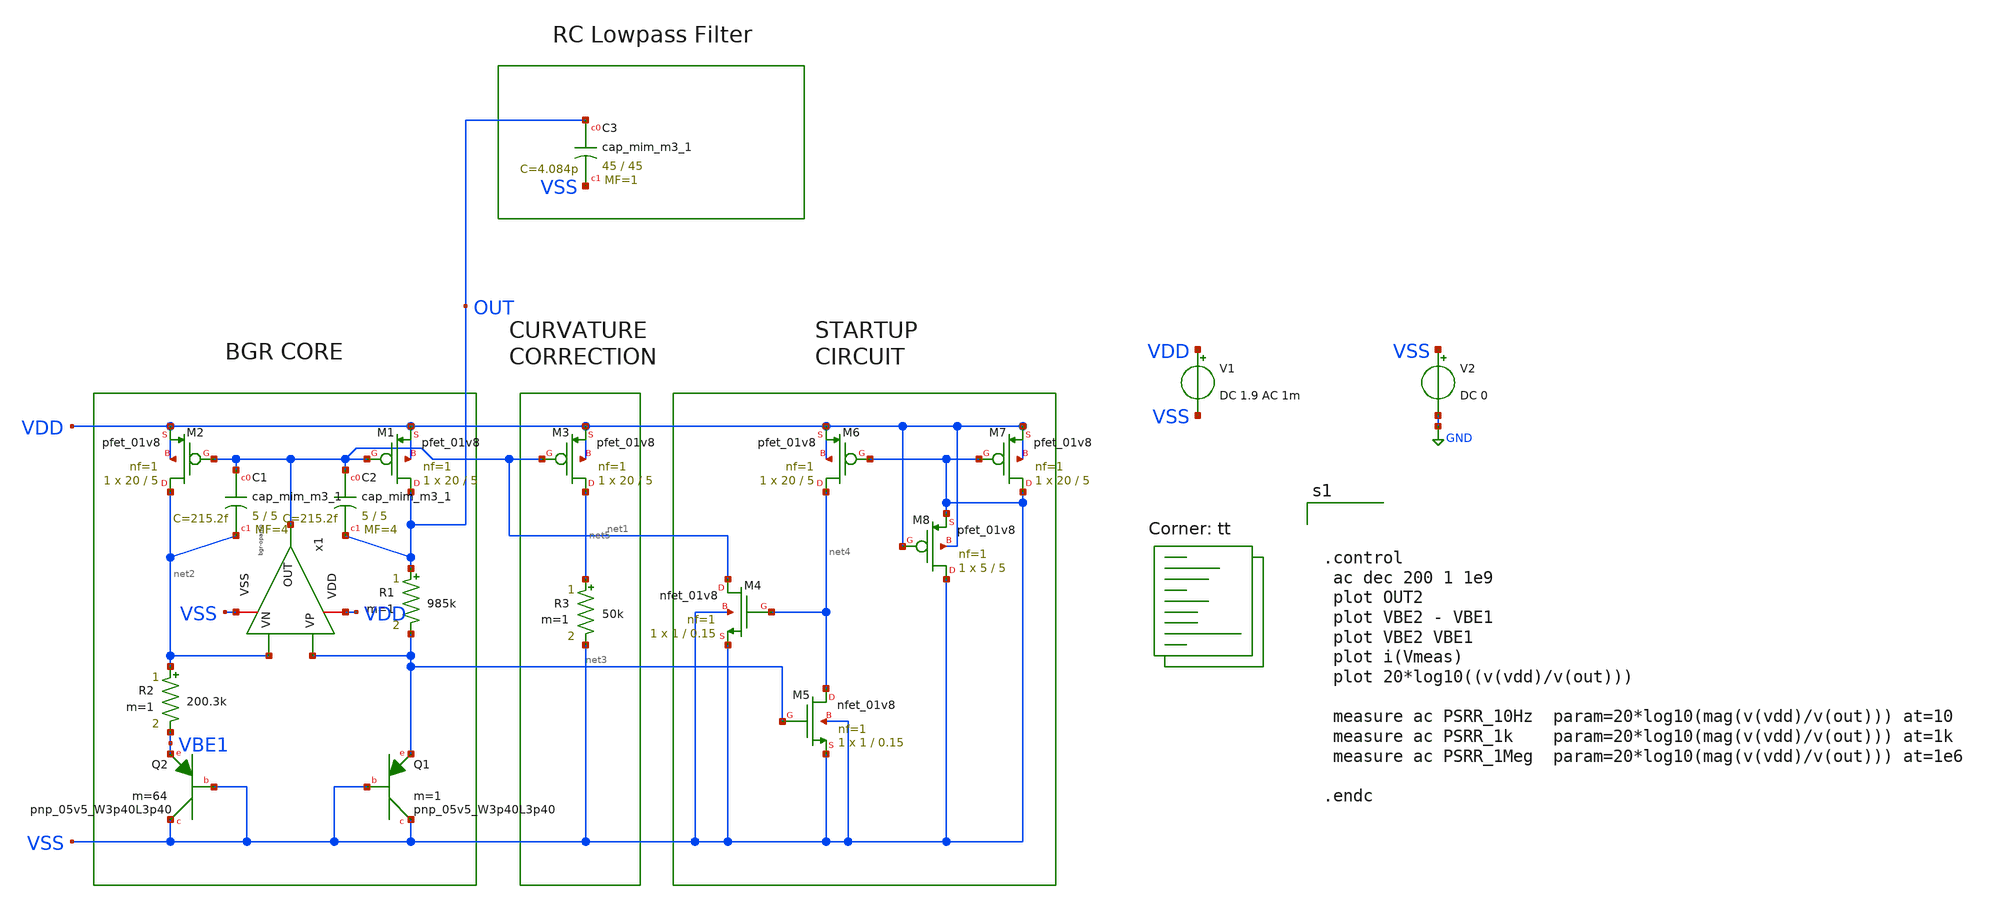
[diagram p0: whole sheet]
** sch_path: bandgap/bgr2-ac.sch
**.subckt bgr2-ac
XM1 OUT net1 VDD VDD sky130_fd_pr__pfet_01v8 L=5 W=20 nf=1 ad='int((nf+1)/2) * W/nf * 0.29' as='int((nf+2)/2) * W/nf * 0.29'
+ pd='2*int((nf+1)/2) * (W/nf + 0.29)' ps='2*int((nf+2)/2) * (W/nf + 0.29)' nrd='0.29 / W' nrs='0.29 / W'
+ sa=0 sb=0 sd=0 mult=1 m=1
XM2 net2 net1 VDD VDD sky130_fd_pr__pfet_01v8 L=5 W=20 nf=1 ad='int((nf+1)/2) * W/nf * 0.29' as='int((nf+2)/2) * W/nf * 0.29'
+ pd='2*int((nf+1)/2) * (W/nf + 0.29)' ps='2*int((nf+2)/2) * (W/nf + 0.29)' nrd='0.29 / W' nrs='0.29 / W'
+ sa=0 sb=0 sd=0 mult=1 m=1
R1 OUT net3 985k m=1
R2 net2 VBE1 200.3k m=1
XQ1 VSS VSS net3 sky130_fd_pr__pnp_05v5_W3p40L3p40 m=1
XQ2 VSS VSS VBE1 sky130_fd_pr__pnp_05v5_W3p40L3p40 m=64
V1 VDD VSS DC 1.9 AC 1m
V2 VSS GND DC 0
XM3 net5 net1 VDD VDD sky130_fd_pr__pfet_01v8 L=5 W=20 nf=1 ad='int((nf+1)/2) * W/nf * 0.29' as='int((nf+2)/2) * W/nf * 0.29'
+ pd='2*int((nf+1)/2) * (W/nf + 0.29)' ps='2*int((nf+2)/2) * (W/nf + 0.29)' nrd='0.29 / W' nrs='0.29 / W'
+ sa=0 sb=0 sd=0 mult=1 m=1
R3 net5 VSS 50k m=1
XM4 net1 net4 VSS VSS sky130_fd_pr__nfet_01v8 L=0.15 W=1 nf=1 ad='int((nf+1)/2) * W/nf * 0.29' as='int((nf+2)/2) * W/nf * 0.29'
+ pd='2*int((nf+1)/2) * (W/nf + 0.29)' ps='2*int((nf+2)/2) * (W/nf + 0.29)' nrd='0.29 / W' nrs='0.29 / W'
+ sa=0 sb=0 sd=0 mult=1 m=1
XM5 net4 net3 VSS VSS sky130_fd_pr__nfet_01v8 L=0.15 W=1 nf=1 ad='int((nf+1)/2) * W/nf * 0.29' as='int((nf+2)/2) * W/nf * 0.29'
+ pd='2*int((nf+1)/2) * (W/nf + 0.29)' ps='2*int((nf+2)/2) * (W/nf + 0.29)' nrd='0.29 / W' nrs='0.29 / W'
+ sa=0 sb=0 sd=0 mult=1 m=1
XM6 net4 VSS VDD VDD sky130_fd_pr__pfet_01v8 L=5 W=20 nf=1 ad='int((nf+1)/2) * W/nf * 0.29' as='int((nf+2)/2) * W/nf * 0.29'
+ pd='2*int((nf+1)/2) * (W/nf + 0.29)' ps='2*int((nf+2)/2) * (W/nf + 0.29)' nrd='0.29 / W' nrs='0.29 / W'
+ sa=0 sb=0 sd=0 mult=1 m=1
XM7 VSS VSS VDD VDD sky130_fd_pr__pfet_01v8 L=5 W=20 nf=1 ad='int((nf+1)/2) * W/nf * 0.29' as='int((nf+2)/2) * W/nf * 0.29'
+ pd='2*int((nf+1)/2) * (W/nf + 0.29)' ps='2*int((nf+2)/2) * (W/nf + 0.29)' nrd='0.29 / W' nrs='0.29 / W'
+ sa=0 sb=0 sd=0 mult=1 m=1
XM8 VSS VDD VSS VDD sky130_fd_pr__pfet_01v8 L=5 W=5 nf=1 ad='int((nf+1)/2) * W/nf * 0.29' as='int((nf+2)/2) * W/nf * 0.29'
+ pd='2*int((nf+1)/2) * (W/nf + 0.29)' ps='2*int((nf+2)/2) * (W/nf + 0.29)' nrd='0.29 / W' nrs='0.29 / W'
+ sa=0 sb=0 sd=0 mult=1 m=1
x1 VDD net1 net3 net2 VSS bgr-opamp
XC1 net1 net2 sky130_fd_pr__cap_mim_m3_1 W=5 L=5 MF=4 m=4
XC2 net1 OUT sky130_fd_pr__cap_mim_m3_1 W=5 L=5 MF=4 m=4
XC3 OUT VSS sky130_fd_pr__cap_mim_m3_1 W=45 L=45 MF=1 m=1
**** begin user architecture code
.lib $::SKYWATER_MODELS/sky130.lib.spice tt



.control
 ac dec 200 1 1e9
 plot OUT2
 plot VBE2 - VBE1
 plot VBE2 VBE1
 plot i(Vmeas)
 plot 20*log10((v(vdd)/v(out)))

 measure ac PSRR_10Hz  param=20*log10(mag(v(vdd)/v(out))) at=10
 measure ac PSRR_1k    param=20*log10(mag(v(vdd)/v(out))) at=1k
 measure ac PSRR_1Meg  param=20*log10(mag(v(vdd)/v(out))) at=1e6

.endc


**** end user architecture code
**.ends

* expanding   symbol:  /foss/designs/afe-icdec-teknofest-2026/bandgap/bgr-opamp/bgr-opamp.sym # of
*+ pins=5
** sym_path: bandgap/bgr-opamp/bgr-opamp.sym
** sch_path: bandgap/bgr-opamp/bgr-opamp.sch
.subckt bgr-opamp VDD OUT VP VN VSS
*.iopin VSS
*.iopin VDD
*.ipin VP
*.ipin VN
*.opin OUT
XM1 net1 VP net3 VSS sky130_fd_pr__nfet_01v8 L=0.3 W=2.5 nf=2 ad='int((nf+1)/2) * W/nf * 0.29' as='int((nf+2)/2) * W/nf * 0.29'
+ pd='2*int((nf+1)/2) * (W/nf + 0.29)' ps='2*int((nf+2)/2) * (W/nf + 0.29)' nrd='0.29 / W' nrs='0.29 / W'
+ sa=0 sb=0 sd=0 mult=1 m=1
XM2 net2 VN net3 VSS sky130_fd_pr__nfet_01v8 L=0.3 W=2.5 nf=2 ad='int((nf+1)/2) * W/nf * 0.29' as='int((nf+2)/2) * W/nf * 0.29'
+ pd='2*int((nf+1)/2) * (W/nf + 0.29)' ps='2*int((nf+2)/2) * (W/nf + 0.29)' nrd='0.29 / W' nrs='0.29 / W'
+ sa=0 sb=0 sd=0 mult=1 m=1
XM4 net2 net1 VDD VDD sky130_fd_pr__pfet_01v8 L=1.25 W=10.8 nf=4 ad='int((nf+1)/2) * W/nf * 0.29' as='int((nf+2)/2) * W/nf * 0.29'
+ pd='2*int((nf+1)/2) * (W/nf + 0.29)' ps='2*int((nf+2)/2) * (W/nf + 0.29)' nrd='0.29 / W' nrs='0.29 / W'
+ sa=0 sb=0 sd=0 mult=1 m=1
XM3 net1 net1 VDD VDD sky130_fd_pr__pfet_01v8 L=1.25 W=10.8 nf=4 ad='int((nf+1)/2) * W/nf * 0.29' as='int((nf+2)/2) * W/nf * 0.29'
+ pd='2*int((nf+1)/2) * (W/nf + 0.29)' ps='2*int((nf+2)/2) * (W/nf + 0.29)' nrd='0.29 / W' nrs='0.29 / W'
+ sa=0 sb=0 sd=0 mult=1 m=1
XM5 net3 net4 VSS VSS sky130_fd_pr__nfet_01v8 L=1.25 W=3.4 nf=1 ad='int((nf+1)/2) * W/nf * 0.29' as='int((nf+2)/2) * W/nf * 0.29'
+ pd='2*int((nf+1)/2) * (W/nf + 0.29)' ps='2*int((nf+2)/2) * (W/nf + 0.29)' nrd='0.29 / W' nrs='0.29 / W'
+ sa=0 sb=0 sd=0 mult=1 m=1
XM9 net4 net5 net10 VSS sky130_fd_pr__nfet_01v8 L=1.25 W=3.4 nf=1 ad='int((nf+1)/2) * W/nf * 0.29' as='int((nf+2)/2) * W/nf * 0.29'
+ pd='2*int((nf+1)/2) * (W/nf + 0.29)' ps='2*int((nf+2)/2) * (W/nf + 0.29)' nrd='0.29 / W' nrs='0.29 / W'
+ sa=0 sb=0 sd=0 mult=1 m=1
XM8 net4 net4 VDD VDD sky130_fd_pr__pfet_01v8 L=1.25 W=10.8 nf=4 ad='int((nf+1)/2) * W/nf * 0.29' as='int((nf+2)/2) * W/nf * 0.29'
+ pd='2*int((nf+1)/2) * (W/nf + 0.29)' ps='2*int((nf+2)/2) * (W/nf + 0.29)' nrd='0.29 / W' nrs='0.29 / W'
+ sa=0 sb=0 sd=0 mult=1 m=1
XM11 net5 net4 VDD VDD sky130_fd_pr__pfet_01v8 L=1.25 W=10.8 nf=4 ad='int((nf+1)/2) * W/nf * 0.29' as='int((nf+2)/2) * W/nf * 0.29'
+ pd='2*int((nf+1)/2) * (W/nf + 0.29)' ps='2*int((nf+2)/2) * (W/nf + 0.29)' nrd='0.29 / W' nrs='0.29 / W'
+ sa=0 sb=0 sd=0 mult=1 m=1
XM10 net5 net5 VSS VSS sky130_fd_pr__nfet_01v8 L=1.25 W=3.4 nf=1 ad='int((nf+1)/2) * W/nf * 0.29' as='int((nf+2)/2) * W/nf * 0.29'
+ pd='2*int((nf+1)/2) * (W/nf + 0.29)' ps='2*int((nf+2)/2) * (W/nf + 0.29)' nrd='0.29 / W' nrs='0.29 / W'
+ sa=0 sb=0 sd=0 mult=1 m=1
XM6 OUT net2 VDD VDD sky130_fd_pr__pfet_01v8 L=1.25 W=110 nf=32 ad='int((nf+1)/2) * W/nf * 0.29' as='int((nf+2)/2) * W/nf * 0.29'
+ pd='2*int((nf+1)/2) * (W/nf + 0.29)' ps='2*int((nf+2)/2) * (W/nf + 0.29)' nrd='0.29 / W' nrs='0.29 / W'
+ sa=0 sb=0 sd=0 mult=1 m=1
XM7 OUT net4 VSS VSS sky130_fd_pr__nfet_01v8 L=1.25 W=12 nf=4 ad='int((nf+1)/2) * W/nf * 0.29' as='int((nf+2)/2) * W/nf * 0.29'
+ pd='2*int((nf+1)/2) * (W/nf + 0.29)' ps='2*int((nf+2)/2) * (W/nf + 0.29)' nrd='0.29 / W' nrs='0.29 / W'
+ sa=0 sb=0 sd=0 mult=1 m=1
XC2 OUT net2 sky130_fd_pr__cap_mim_m3_1 W=15 L=15 MF=4 m=4
XM12 net4 net4 net5 VSS sky130_fd_pr__nfet_01v8 L=0.15 W=0.85 nf=1 ad='int((nf+1)/2) * W/nf * 0.29' as='int((nf+2)/2) * W/nf * 0.29'
+ pd='2*int((nf+1)/2) * (W/nf + 0.29)' ps='2*int((nf+2)/2) * (W/nf + 0.29)' nrd='0.29 / W' nrs='0.29 / W'
+ sa=0 sb=0 sd=0 mult=1 m=1
XR2 net6 net10 VSS sky130_fd_pr__res_high_po_1p41 L=3.235 mult=1 m=1
XR3 net8 net6 VSS sky130_fd_pr__res_high_po_1p41 L=3.235 mult=1 m=1
XR4 net7 net8 VSS sky130_fd_pr__res_high_po_1p41 L=3.235 mult=1 m=1
XR5 net9 net7 VSS sky130_fd_pr__res_high_po_1p41 L=3.235 mult=1 m=1
XR6 VSS net9 VSS sky130_fd_pr__res_high_po_1p41 L=3.235 mult=1 m=1
.ends

.GLOBAL GND
.end
